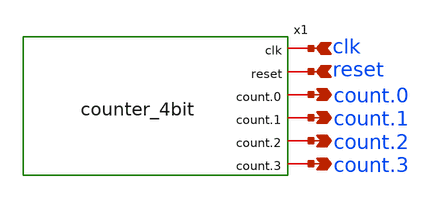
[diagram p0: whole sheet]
** sch_path: units/top/ana/blocks/counter_4bit/untitled.sch
**.subckt untitled clk count.2 count.1 count.3 count.0 reset
*.ipin clk
*.opin count.2
*.opin count.1
*.opin count.3
*.opin count.0
*.ipin reset
**** begin user architecture code


* include sky130 HD standard cell spice models
.include /home/jihan/eda/open_pdks/sky130/sky130A/libs.ref/sky130_fd_sc_hd/spice/sky130_fd_sc_hd.spice

* include synthesized counter netlist
.include /home/jihan/projects/units/top/sim/synth/counter_4bit_xschem.spice

* instantiate the counter (7 pins: clk reset count.0..3 VGND)
XU1 clk reset count.0 count.1 count.2 count.3 0 counter_4bit

* stimulus
VCLK   clk   0  PULSE(0 1.8 0 100p 100p 5n 10n)
VRESET reset 0  PULSE(1.8 0 0 100p 100p 20n 100n)

.tran 0.1n 200n


**** end user architecture code
**.ends
.end
